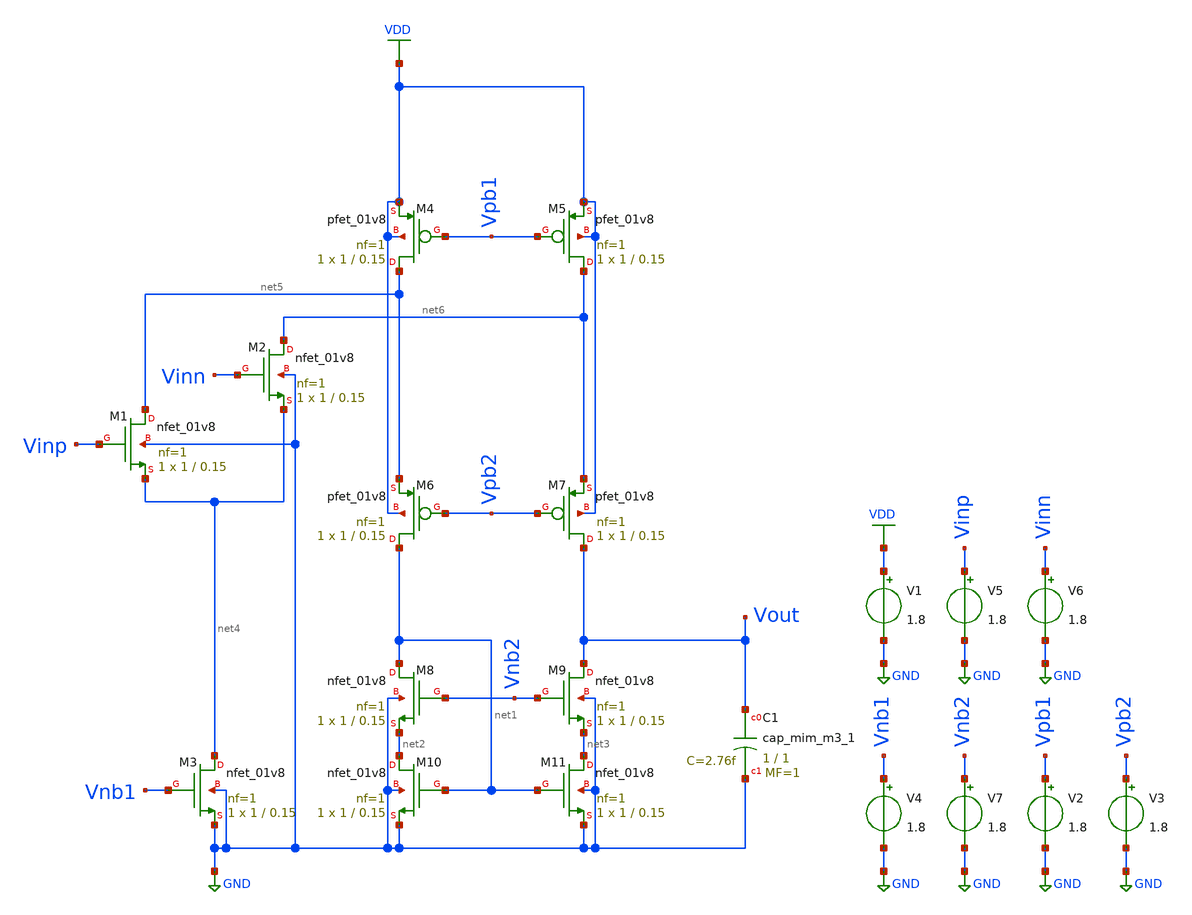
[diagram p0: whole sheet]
** sch_path: opamp_design/folded_cascode_opamp/folded_cascode_opamp.sch
**.subckt folded_cascode_opamp
XM11 net3 net1 GND GND sky130_fd_pr__nfet_01v8 L=0.15 W=1 nf=1 ad='int((nf+1)/2) * W/nf * 0.29' as='int((nf+2)/2) * W/nf * 0.29'
+ pd='2*int((nf+1)/2) * (W/nf + 0.29)' ps='2*int((nf+2)/2) * (W/nf + 0.29)' nrd='0.29 / W' nrs='0.29 / W'
+ sa=0 sb=0 sd=0 mult=1 m=1
XM10 net2 net1 GND GND sky130_fd_pr__nfet_01v8 L=0.15 W=1 nf=1 ad='int((nf+1)/2) * W/nf * 0.29' as='int((nf+2)/2) * W/nf * 0.29'
+ pd='2*int((nf+1)/2) * (W/nf + 0.29)' ps='2*int((nf+2)/2) * (W/nf + 0.29)' nrd='0.29 / W' nrs='0.29 / W'
+ sa=0 sb=0 sd=0 mult=1 m=1
XM8 net1 Vnb2 net2 GND sky130_fd_pr__nfet_01v8 L=0.15 W=1 nf=1 ad='int((nf+1)/2) * W/nf * 0.29' as='int((nf+2)/2) * W/nf * 0.29'
+ pd='2*int((nf+1)/2) * (W/nf + 0.29)' ps='2*int((nf+2)/2) * (W/nf + 0.29)' nrd='0.29 / W' nrs='0.29 / W'
+ sa=0 sb=0 sd=0 mult=1 m=1
XM9 Vout Vnb2 net3 GND sky130_fd_pr__nfet_01v8 L=0.15 W=1 nf=1 ad='int((nf+1)/2) * W/nf * 0.29' as='int((nf+2)/2) * W/nf * 0.29'
+ pd='2*int((nf+1)/2) * (W/nf + 0.29)' ps='2*int((nf+2)/2) * (W/nf + 0.29)' nrd='0.29 / W' nrs='0.29 / W'
+ sa=0 sb=0 sd=0 mult=1 m=1
XM7 Vout Vpb2 net6 VDD sky130_fd_pr__pfet_01v8 L=0.15 W=1 nf=1 ad='int((nf+1)/2) * W/nf * 0.29' as='int((nf+2)/2) * W/nf * 0.29'
+ pd='2*int((nf+1)/2) * (W/nf + 0.29)' ps='2*int((nf+2)/2) * (W/nf + 0.29)' nrd='0.29 / W' nrs='0.29 / W'
+ sa=0 sb=0 sd=0 mult=1 m=1
XM6 net1 Vpb2 net5 VDD sky130_fd_pr__pfet_01v8 L=0.15 W=1 nf=1 ad='int((nf+1)/2) * W/nf * 0.29' as='int((nf+2)/2) * W/nf * 0.29'
+ pd='2*int((nf+1)/2) * (W/nf + 0.29)' ps='2*int((nf+2)/2) * (W/nf + 0.29)' nrd='0.29 / W' nrs='0.29 / W'
+ sa=0 sb=0 sd=0 mult=1 m=1
XM1 net5 Vinp net4 GND sky130_fd_pr__nfet_01v8 L=0.15 W=1 nf=1 ad='int((nf+1)/2) * W/nf * 0.29' as='int((nf+2)/2) * W/nf * 0.29'
+ pd='2*int((nf+1)/2) * (W/nf + 0.29)' ps='2*int((nf+2)/2) * (W/nf + 0.29)' nrd='0.29 / W' nrs='0.29 / W'
+ sa=0 sb=0 sd=0 mult=1 m=1
XM2 net6 Vinn net4 GND sky130_fd_pr__nfet_01v8 L=0.15 W=1 nf=1 ad='int((nf+1)/2) * W/nf * 0.29' as='int((nf+2)/2) * W/nf * 0.29'
+ pd='2*int((nf+1)/2) * (W/nf + 0.29)' ps='2*int((nf+2)/2) * (W/nf + 0.29)' nrd='0.29 / W' nrs='0.29 / W'
+ sa=0 sb=0 sd=0 mult=1 m=1
XM3 net4 Vnb1 GND GND sky130_fd_pr__nfet_01v8 L=0.15 W=1 nf=1 ad='int((nf+1)/2) * W/nf * 0.29' as='int((nf+2)/2) * W/nf * 0.29'
+ pd='2*int((nf+1)/2) * (W/nf + 0.29)' ps='2*int((nf+2)/2) * (W/nf + 0.29)' nrd='0.29 / W' nrs='0.29 / W'
+ sa=0 sb=0 sd=0 mult=1 m=1
XM4 net5 Vpb1 VDD VDD sky130_fd_pr__pfet_01v8 L=0.15 W=1 nf=1 ad='int((nf+1)/2) * W/nf * 0.29' as='int((nf+2)/2) * W/nf * 0.29'
+ pd='2*int((nf+1)/2) * (W/nf + 0.29)' ps='2*int((nf+2)/2) * (W/nf + 0.29)' nrd='0.29 / W' nrs='0.29 / W'
+ sa=0 sb=0 sd=0 mult=1 m=1
XM5 net6 Vpb1 VDD VDD sky130_fd_pr__pfet_01v8 L=0.15 W=1 nf=1 ad='int((nf+1)/2) * W/nf * 0.29' as='int((nf+2)/2) * W/nf * 0.29'
+ pd='2*int((nf+1)/2) * (W/nf + 0.29)' ps='2*int((nf+2)/2) * (W/nf + 0.29)' nrd='0.29 / W' nrs='0.29 / W'
+ sa=0 sb=0 sd=0 mult=1 m=1
V1 VDD GND 1.8
V2 Vpb1 GND 1.8
V3 Vpb2 GND 1.8
V4 Vnb1 GND 1.8
V5 Vinp GND 1.8
V6 Vinn GND 1.8
XC1 Vout GND sky130_fd_pr__cap_mim_m3_1 W=1 L=1 MF=1 m=1
V7 Vnb2 GND 1.8
**.ends
.GLOBAL VDD
.GLOBAL GND
.end
